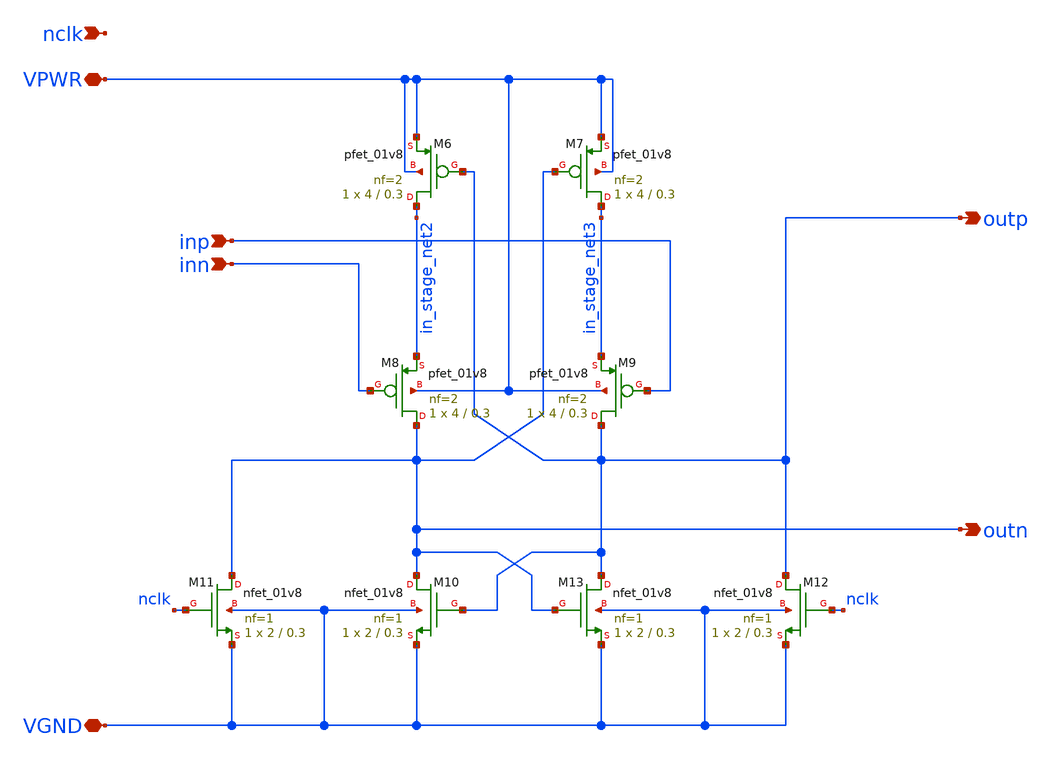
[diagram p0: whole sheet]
** sch_path: Circuits/Comparator/Comp.sch
**.subckt Comp outp outn VPWR nclk VGND inp inn
*.opin outp
*.opin outn
*.iopin VPWR
*.ipin nclk
*.iopin VGND
*.ipin inp
*.ipin inn
XM6 in_stage_net2 outp VPWR VPWR sky130_fd_pr__pfet_01v8 L=0.3 W=4 nf=2 ad='int((nf+1)/2) * W/nf * 0.29'
+ as='int((nf+2)/2) * W/nf * 0.29' pd='2*int((nf+1)/2) * (W/nf + 0.29)' ps='2*int((nf+2)/2) * (W/nf + 0.29)'
+ nrd='0.29 / W' nrs='0.29 / W' sa=0 sb=0 sd=0 mult=1 m=1
XM7 in_stage_net3 outn VPWR VPWR sky130_fd_pr__pfet_01v8 L=0.3 W=4 nf=2 ad='int((nf+1)/2) * W/nf * 0.29'
+ as='int((nf+2)/2) * W/nf * 0.29' pd='2*int((nf+1)/2) * (W/nf + 0.29)' ps='2*int((nf+2)/2) * (W/nf + 0.29)'
+ nrd='0.29 / W' nrs='0.29 / W' sa=0 sb=0 sd=0 mult=1 m=1
XM8 outn inn in_stage_net2 VPWR sky130_fd_pr__pfet_01v8 L=0.3 W=4 nf=2 ad='int((nf+1)/2) * W/nf * 0.29'
+ as='int((nf+2)/2) * W/nf * 0.29' pd='2*int((nf+1)/2) * (W/nf + 0.29)' ps='2*int((nf+2)/2) * (W/nf + 0.29)'
+ nrd='0.29 / W' nrs='0.29 / W' sa=0 sb=0 sd=0 mult=1 m=1
XM9 outp inp in_stage_net3 VPWR sky130_fd_pr__pfet_01v8 L=0.3 W=4 nf=2 ad='int((nf+1)/2) * W/nf * 0.29'
+ as='int((nf+2)/2) * W/nf * 0.29' pd='2*int((nf+1)/2) * (W/nf + 0.29)' ps='2*int((nf+2)/2) * (W/nf + 0.29)'
+ nrd='0.29 / W' nrs='0.29 / W' sa=0 sb=0 sd=0 mult=1 m=1
XM10 outn outp VGND VGND sky130_fd_pr__nfet_01v8 L=0.3 W=2 nf=1 ad='int((nf+1)/2) * W/nf * 0.29' as='int((nf+2)/2) * W/nf * 0.29'
+ pd='2*int((nf+1)/2) * (W/nf + 0.29)' ps='2*int((nf+2)/2) * (W/nf + 0.29)' nrd='0.29 / W' nrs='0.29 / W'
+ sa=0 sb=0 sd=0 mult=1 m=1
XM11 outn nclk VGND VGND sky130_fd_pr__nfet_01v8 L=0.3 W=2 nf=1 ad='int((nf+1)/2) * W/nf * 0.29' as='int((nf+2)/2) * W/nf * 0.29'
+ pd='2*int((nf+1)/2) * (W/nf + 0.29)' ps='2*int((nf+2)/2) * (W/nf + 0.29)' nrd='0.29 / W' nrs='0.29 / W'
+ sa=0 sb=0 sd=0 mult=1 m=1
XM12 outp nclk VGND VGND sky130_fd_pr__nfet_01v8 L=0.3 W=2 nf=1 ad='int((nf+1)/2) * W/nf * 0.29' as='int((nf+2)/2) * W/nf * 0.29'
+ pd='2*int((nf+1)/2) * (W/nf + 0.29)' ps='2*int((nf+2)/2) * (W/nf + 0.29)' nrd='0.29 / W' nrs='0.29 / W'
+ sa=0 sb=0 sd=0 mult=1 m=1
XM13 outp outn VGND VGND sky130_fd_pr__nfet_01v8 L=0.3 W=2 nf=1 ad='int((nf+1)/2) * W/nf * 0.29' as='int((nf+2)/2) * W/nf * 0.29'
+ pd='2*int((nf+1)/2) * (W/nf + 0.29)' ps='2*int((nf+2)/2) * (W/nf + 0.29)' nrd='0.29 / W' nrs='0.29 / W'
+ sa=0 sb=0 sd=0 mult=1 m=1
**.ends
.end
